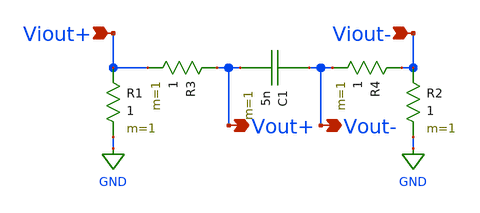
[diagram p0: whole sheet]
** sch_path: simulation/filter/filter.sch
**.subckt filter Vout+ Vout- Viout+ Viout-
*.opin Vout+
*.opin Vout-
*.ipin Viout+
*.ipin Viout-
R1 Viout+ GND 1 m=1
R2 Viout- GND 1 m=1
R3 Vout+ Viout+ 1 m=1
R4 Viout- Vout- 1 m=1
C1 Vout- Vout+ 5n m=1
**.ends
.GLOBAL GND
.end
